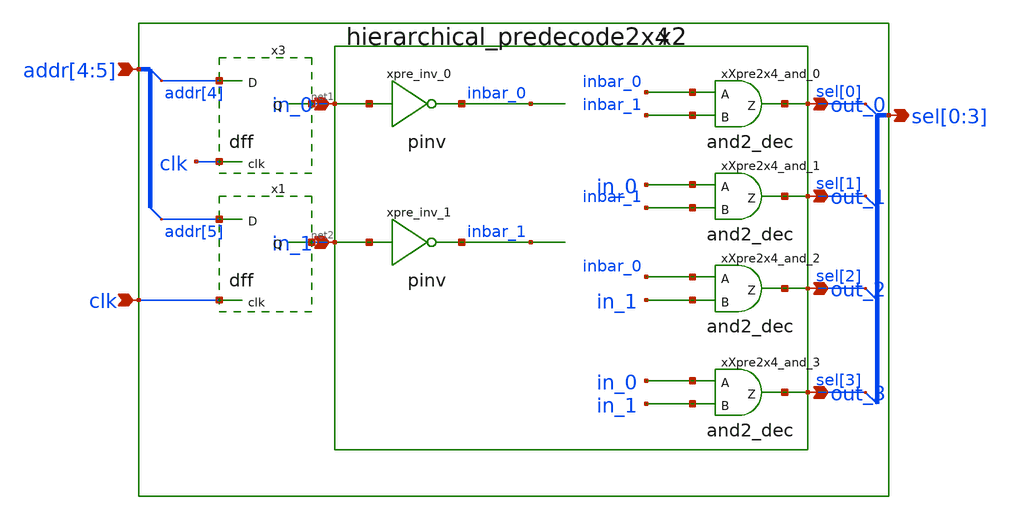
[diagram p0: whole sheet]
** sch_path: sram_2_64_scn4m_lcc/col_decoder.sch
**.subckt col_decoder addr[4],addr[5] clk sel[0],sel[1],sel[2],sel[3]
*.ipin addr[4],addr[5]
*.ipin clk
*.opin sel[0],sel[1],sel[2],sel[3]
x2 net1 net2 sel[0] sel[1] sel[2] sel[3] vdd gnd hierarchical_predecode2x4
x3 addr[4] net1 clk vdd gnd dff
x1 addr[5] net2 clk vdd gnd dff
**.ends

* expanding   symbol:  hierarchical_predecode2x4.sch # of pins=6
** sym_path: sram_2_64_scn4m_lcc/hierarchical_predecode2x4.sch
** sch_path: sram_2_64_scn4m_lcc/hierarchical_predecode2x4.sch
.subckt hierarchical_predecode2x4 in_0 in_1 out_0 out_1 out_2 out_3 vdd gnd
*.ipin in_0
*.ipin in_1
*.opin out_0
*.opin out_1
*.opin out_2
*.opin out_3
xpre_inv_0 in_0 inbar_0 vdd gnd pinv
xpre_inv_1 in_1 inbar_1 vdd gnd pinv
xXpre2x4_and_0 inbar_0 inbar_1 out_0 and2_dec
xXpre2x4_and_1 in_0 inbar_1 out_1 and2_dec
xXpre2x4_and_2 inbar_0 in_1 out_2 and2_dec
xXpre2x4_and_3 in_0 in_1 out_3 and2_dec
.ends


* expanding   symbol:  dff.sym # of pins=3
** sym_path: sram_2_64_scn4m_lcc/dff.sym
** sch_path: sram_2_64_scn4m_lcc/dff.sch
.subckt dff D Q clk vdd gnd
*.ipin D
*.ipin clk
*.opin Q
M1013 net1 a_24_24# net2 gnd n w=5u l=0.18u m=1
M1012 net2 D gnd gnd n w=2u l=0.4u m=1
M1001 net3 D vdd vdd p w=4u l=0.4u m=1
M1002 net1 clk net3 vdd p w=4u l=0.4u m=1
M1000 a_24_24# clk vdd vdd p w=8u l=0.4u m=1
M1010 a_24_24# clk gnd gnd n w=4u l=0.4u m=1
M1005 a_152_16# net1 vdd vdd p w=4u l=0.4u m=1
M1016 a_152_16# net1 gnd gnd n w=5u l=0.4u m=1
M1004 net5 a_152_16# vdd vdd p w=4u l=0.4u m=1
M1003 net1 a_24_24# net5 vdd p w=4u l=0.4u m=1
M1014 net1 clk net4 gnd n w=2u l=0.4u m=1
M1015 net4 a_152_16# gnd gnd n w=2u l=0.4u m=1
M1006 net8 a_152_16# vdd vdd p w=4u l=0.4u m=1
M1007 net6 a_24_24# net8 vdd p w=4u l=0.4u m=1
M1018 net6 clk net7 gnd n w=2u l=0.4u m=1
M1017 net7 a_152_16# gnd gnd n w=2u l=0.4u m=1
M1021 Q net6 gnd gnd n w=4u l=0.4u m=1
M1011 Q net6 vdd vdd p w=8u l=0.4u m=1
M1020 net9 Q gnd gnd n w=2u l=0.4u m=1
M1019 net6 a_24_24# net9 gnd n w=2u l=0.4u m=1
M1009 net10 Q vdd vdd p w=2u l=0.4u m=1
M1008 net6 clk net10 vdd p w=2u l=0.4u m=1
.ends


* expanding   symbol:  pinv.sym # of pins=2
** sym_path: sram_4_16_scn4m/pinv.sym
** sch_path: sram_4_16_scn4m/pinv.sch
.subckt pinv A Z vdd gnd
*.ipin A
*.opin Z
Mpinv_nmos Z A gnd gnd n w=0.8u l=0.4u m=1
Mp_inv_pmos Z A vdd vdd p w=1.6u l=0.4u m=1
.ends


* expanding   symbol:  and2_dec.sym # of pins=3
** sym_path: sram_4_16_scn4m/and2_dec.sym
** sch_path: sram_4_16_scn4m/and2_dec.sch
.subckt and2_dec A B Z
*.ipin A
*.ipin B
*.opin Z
xpand2_dec_nand A B zb_int vdd gnd pnand2
xpand2_dec_inv zb_int Z vdd gnd pinv
.ends


* expanding   symbol:  pnand2.sym # of pins=3
** sym_path: sram_2_64_scn4m/pnand2.sym
** sch_path: sram_2_64_scn4m/pnand2.sch
.subckt pnand2 A B Z vdd gnd
*.ipin A
*.ipin B
*.opin Z
*.iopin vdd
*.iopin gnd
XMpnand2_nmos1 Z B net1 gnd sky130_fd_pr__nfet_01v8 L=0.4 W=1.6 nf=1 ad='int((nf+1)/2) * W/nf * 0.29'
+ as='int((nf+2)/2) * W/nf * 0.29' pd='2*int((nf+1)/2) * (W/nf + 0.29)' ps='2*int((nf+2)/2) * (W/nf + 0.29)'
+ nrd='0.29 / W' nrs='0.29 / W' sa=0 sb=0 sd=0 mult=1 m=1
XMpnand2_pmos1 Z A vdd vdd sky130_fd_pr__pfet_01v8 L=0.4 W=1.6 nf=1 ad='int((nf+1)/2) * W/nf * 0.29'
+ as='int((nf+2)/2) * W/nf * 0.29' pd='2*int((nf+1)/2) * (W/nf + 0.29)' ps='2*int((nf+2)/2) * (W/nf + 0.29)'
+ nrd='0.29 / W' nrs='0.29 / W' sa=0 sb=0 sd=0 mult=1 m=1
XMpnand2_pmos2 Z B vdd vdd sky130_fd_pr__pfet_01v8 L=0.4 W=1.6 nf=1 ad='int((nf+1)/2) * W/nf * 0.29'
+ as='int((nf+2)/2) * W/nf * 0.29' pd='2*int((nf+1)/2) * (W/nf + 0.29)' ps='2*int((nf+2)/2) * (W/nf + 0.29)'
+ nrd='0.29 / W' nrs='0.29 / W' sa=0 sb=0 sd=0 mult=1 m=1
XMpnand2_nmos2 net1 A gnd gnd sky130_fd_pr__nfet_01v8 L=0.4 W=1.6 nf=1 ad='int((nf+1)/2) * W/nf * 0.29'
+ as='int((nf+2)/2) * W/nf * 0.29' pd='2*int((nf+1)/2) * (W/nf + 0.29)' ps='2*int((nf+2)/2) * (W/nf + 0.29)'
+ nrd='0.29 / W' nrs='0.29 / W' sa=0 sb=0 sd=0 mult=1 m=1
.ends

.end
